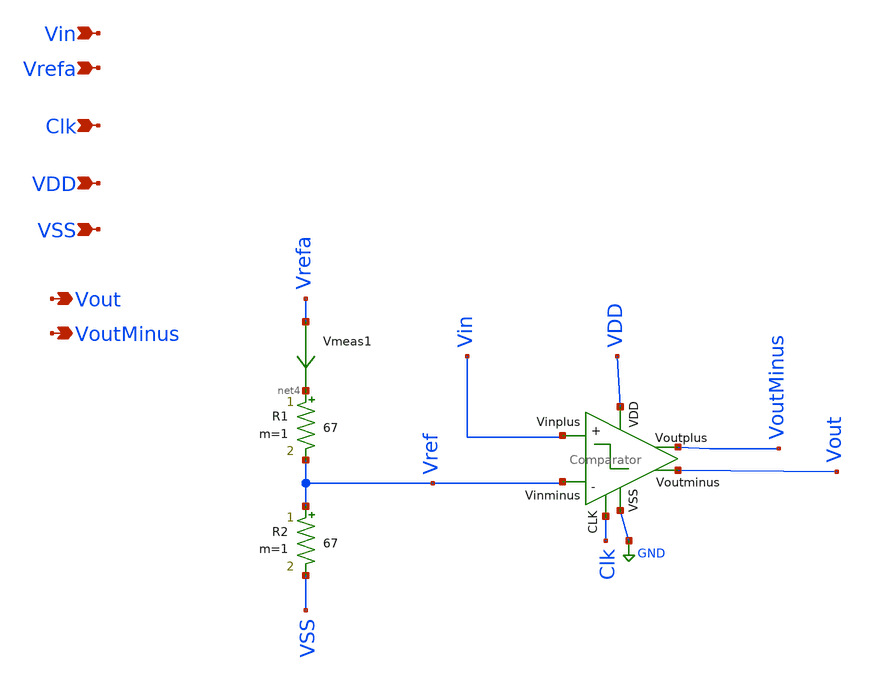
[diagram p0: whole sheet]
** sch_path: xschem/DataConverters/1bitADC.sch
**.subckt 1bitADC Vin Vrefa Clk VDD VSS Vout VoutMinus
*.ipin Vin
*.ipin Vrefa
*.ipin Clk
*.ipin VDD
*.ipin VSS
*.opin Vout
*.opin VoutMinus
x1 VDD Vout VoutMinus net1 net2 net3 GND Comparator
Vmeas1 Vrefa net4 0
.save i(vmeas1)
R1 net4 Vref 67 m=1
R2 Vref VSS 67 m=1
**.ends
.GLOBAL GND
.end
